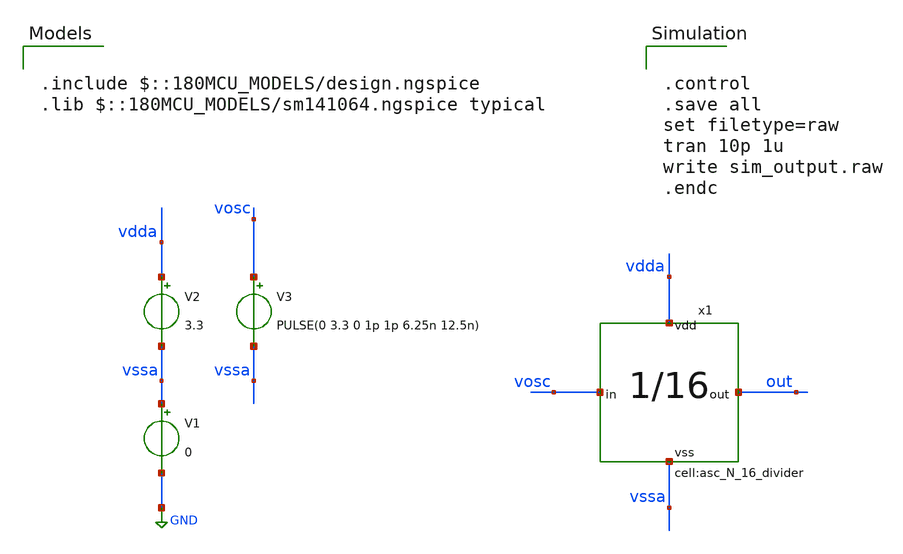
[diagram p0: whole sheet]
** sch_path: designs/libs/xp_tb_analog/tb_asc_N_16_divider/tb_asc_N_16_divider.sch
**.subckt tb_asc_N_16_divider
V1 vssa GND 0
V2 vdda vssa 3.3
V3 vosc vssa PULSE(0 3.3 0 1p 1p 6.25n 12.5n)
x1 vosc out vdda vssa asc_N_16_divider
**** begin user architecture code

.include $::180MCU_MODELS/design.ngspice
.lib $::180MCU_MODELS/sm141064.ngspice typical



.control
.save all
set filetype=raw
tran 10p 1u
write sim_output.raw
.endc


**** end user architecture code
**.ends
.GLOBAL GND
.end
